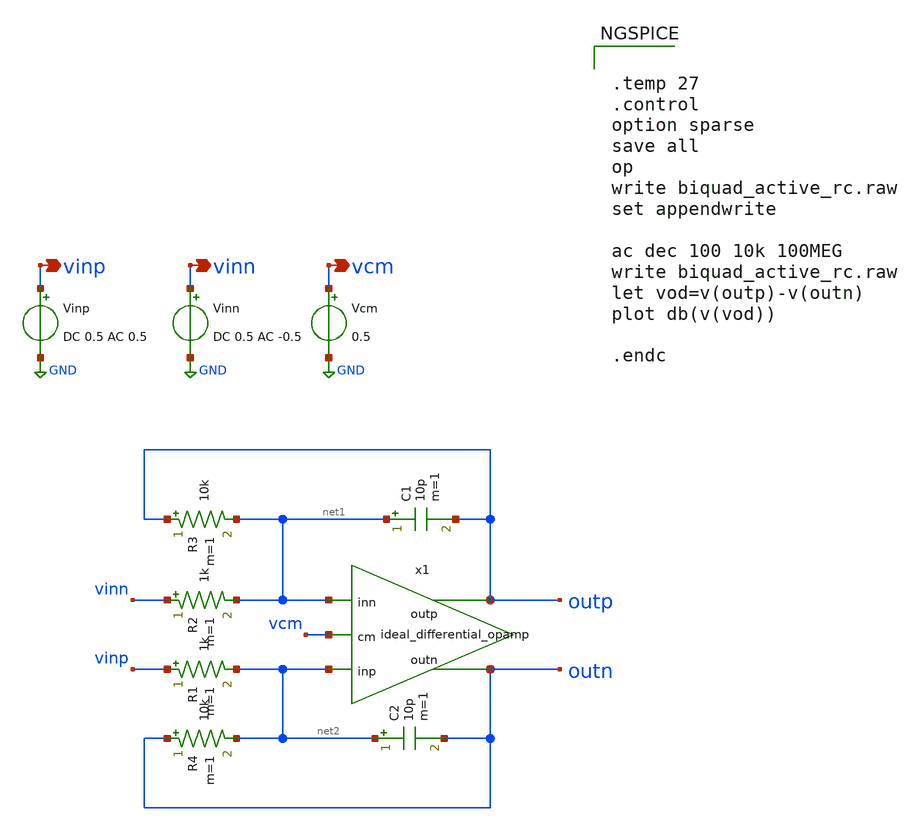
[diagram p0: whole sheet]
** sch_path: prj/template/2_Idealized_circuits/1st_ord_lp_active_rc.sch
**.subckt 1st_ord_lp_active_rc vinp vinn vcm
*.opin vinp
*.opin vinn
*.opin vcm
C1 net1 outp 10p m=1
Vinp vinp GND DC 0.5 AC 0.5
Vinn vinn GND DC 0.5 AC -0.5
Vcm vcm GND 0.5
x1 net2 net1 outp outn vcm ideal_differential_opamp
R1 vinp net2 1k m=1
R2 vinn net1 1k m=1
R3 outp net1 10k m=1
R4 outn net2 10k m=1
C2 net2 outn 10p m=1
**** begin user architecture code


.temp 27
.control
option sparse
save all
op
write biquad_active_rc.raw
set appendwrite

ac dec 100 10k 100MEG
write biquad_active_rc.raw
let vod=v(outp)-v(outn)
plot db(v(vod))

.endc


**** end user architecture code
**.ends

* expanding   symbol:  ideal_differential_opamp.sym # of pins=5
** sym_path: prj/template/2_Idealized_circuits/ideal_differential_opamp.sym
** sch_path: prj/template/2_Idealized_circuits/ideal_differential_opamp.sch
.subckt ideal_differential_opamp inp inn outp outn cm
*.opin outp
*.ipin inp
*.ipin inn
*.opin outn
*.ipin cm
G1 outp net1 inp inn 100Meg
R1 outp net1 1 m=1
G2 net1 outn inp inn 100Meg
R2 net1 outn 1 m=1
G3 net1 GND cm net1 100Meg
.ends

.GLOBAL GND
.end
